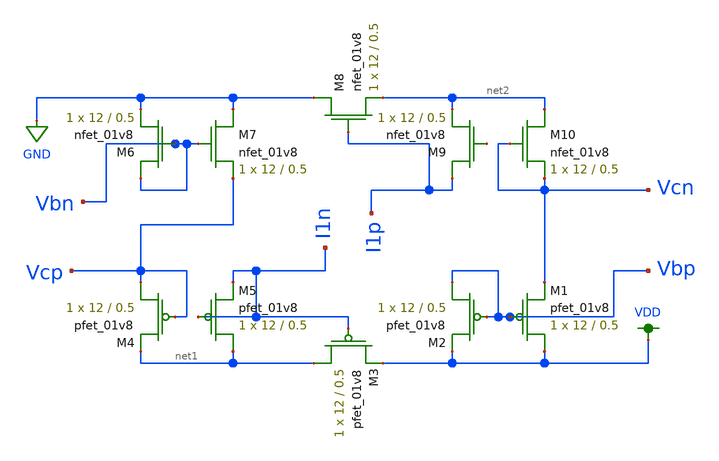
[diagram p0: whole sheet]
** sch_path: bias_abstract.sch
**.subckt bias_abstract
XM1 VDD Vbp Vcn VDD sky130_fd_pr__pfet_01v8 L=0.5 W=12 nf=1 ad='int((nf+1)/2) * W/nf * 0.29' as='int((nf+2)/2) * W/nf * 0.29'
+ pd='2*int((nf+1)/2) * (W/nf + 0.29)' ps='2*int((nf+2)/2) * (W/nf + 0.29)' nrd='0.29 / W' nrs='0.29 / W'
+ sa=0 sb=0 sd=0 mult=1 m=1
XM2 Vbp Vbp VDD VDD sky130_fd_pr__pfet_01v8 L=0.5 W=12 nf=1 ad='int((nf+1)/2) * W/nf * 0.29' as='int((nf+2)/2) * W/nf * 0.29'
+ pd='2*int((nf+1)/2) * (W/nf + 0.29)' ps='2*int((nf+2)/2) * (W/nf + 0.29)' nrd='0.29 / W' nrs='0.29 / W'
+ sa=0 sb=0 sd=0 mult=1 m=1
XM4 Vcp Vcp net1 VDD sky130_fd_pr__pfet_01v8 L=0.5 W=12 nf=1 ad='int((nf+1)/2) * W/nf * 0.29' as='int((nf+2)/2) * W/nf * 0.29'
+ pd='2*int((nf+1)/2) * (W/nf + 0.29)' ps='2*int((nf+2)/2) * (W/nf + 0.29)' nrd='0.29 / W' nrs='0.29 / W'
+ sa=0 sb=0 sd=0 mult=1 m=1
XM6 Vbn Vbn GND GND sky130_fd_pr__nfet_01v8 L=0.5 W=12 nf=1 ad='int((nf+1)/2) * W/nf * 0.29' as='int((nf+2)/2) * W/nf * 0.29'
+ pd='2*int((nf+1)/2) * (W/nf + 0.29)' ps='2*int((nf+2)/2) * (W/nf + 0.29)' nrd='0.29 / W' nrs='0.29 / W'
+ sa=0 sb=0 sd=0 mult=1 m=1
XM7 GND Vbn Vcp GND sky130_fd_pr__nfet_01v8 L=0.5 W=12 nf=1 ad='int((nf+1)/2) * W/nf * 0.29' as='int((nf+2)/2) * W/nf * 0.29'
+ pd='2*int((nf+1)/2) * (W/nf + 0.29)' ps='2*int((nf+2)/2) * (W/nf + 0.29)' nrd='0.29 / W' nrs='0.29 / W'
+ sa=0 sb=0 sd=0 mult=1 m=1
XM8 GND I1p net2 GND sky130_fd_pr__nfet_01v8 L=0.5 W=12 nf=1 ad='int((nf+1)/2) * W/nf * 0.29' as='int((nf+2)/2) * W/nf * 0.29'
+ pd='2*int((nf+1)/2) * (W/nf + 0.29)' ps='2*int((nf+2)/2) * (W/nf + 0.29)' nrd='0.29 / W' nrs='0.29 / W'
+ sa=0 sb=0 sd=0 mult=1 m=1
XM9 I1p net3 net2 GND sky130_fd_pr__nfet_01v8 L=0.5 W=12 nf=1 ad='int((nf+1)/2) * W/nf * 0.29' as='int((nf+2)/2) * W/nf * 0.29'
+ pd='2*int((nf+1)/2) * (W/nf + 0.29)' ps='2*int((nf+2)/2) * (W/nf + 0.29)' nrd='0.29 / W' nrs='0.29 / W'
+ sa=0 sb=0 sd=0 mult=1 m=1
XM10 net2 Vcn Vcn GND sky130_fd_pr__nfet_01v8 L=0.5 W=12 nf=1 ad='int((nf+1)/2) * W/nf * 0.29' as='int((nf+2)/2) * W/nf * 0.29'
+ pd='2*int((nf+1)/2) * (W/nf + 0.29)' ps='2*int((nf+2)/2) * (W/nf + 0.29)' nrd='0.29 / W' nrs='0.29 / W'
+ sa=0 sb=0 sd=0 mult=1 m=1
XM3 net1 I1n VDD VDD sky130_fd_pr__pfet_01v8 L=0.5 W=12 nf=1 ad='int((nf+1)/2) * W/nf * 0.29' as='int((nf+2)/2) * W/nf * 0.29'
+ pd='2*int((nf+1)/2) * (W/nf + 0.29)' ps='2*int((nf+2)/2) * (W/nf + 0.29)' nrd='0.29 / W' nrs='0.29 / W'
+ sa=0 sb=0 sd=0 mult=1 m=1
XM5 net1 I1n I1n VDD sky130_fd_pr__pfet_01v8 L=0.5 W=12 nf=1 ad='int((nf+1)/2) * W/nf * 0.29' as='int((nf+2)/2) * W/nf * 0.29'
+ pd='2*int((nf+1)/2) * (W/nf + 0.29)' ps='2*int((nf+2)/2) * (W/nf + 0.29)' nrd='0.29 / W' nrs='0.29 / W'
+ sa=0 sb=0 sd=0 mult=1 m=1
**.ends
.GLOBAL VDD
.GLOBAL GND
.end
